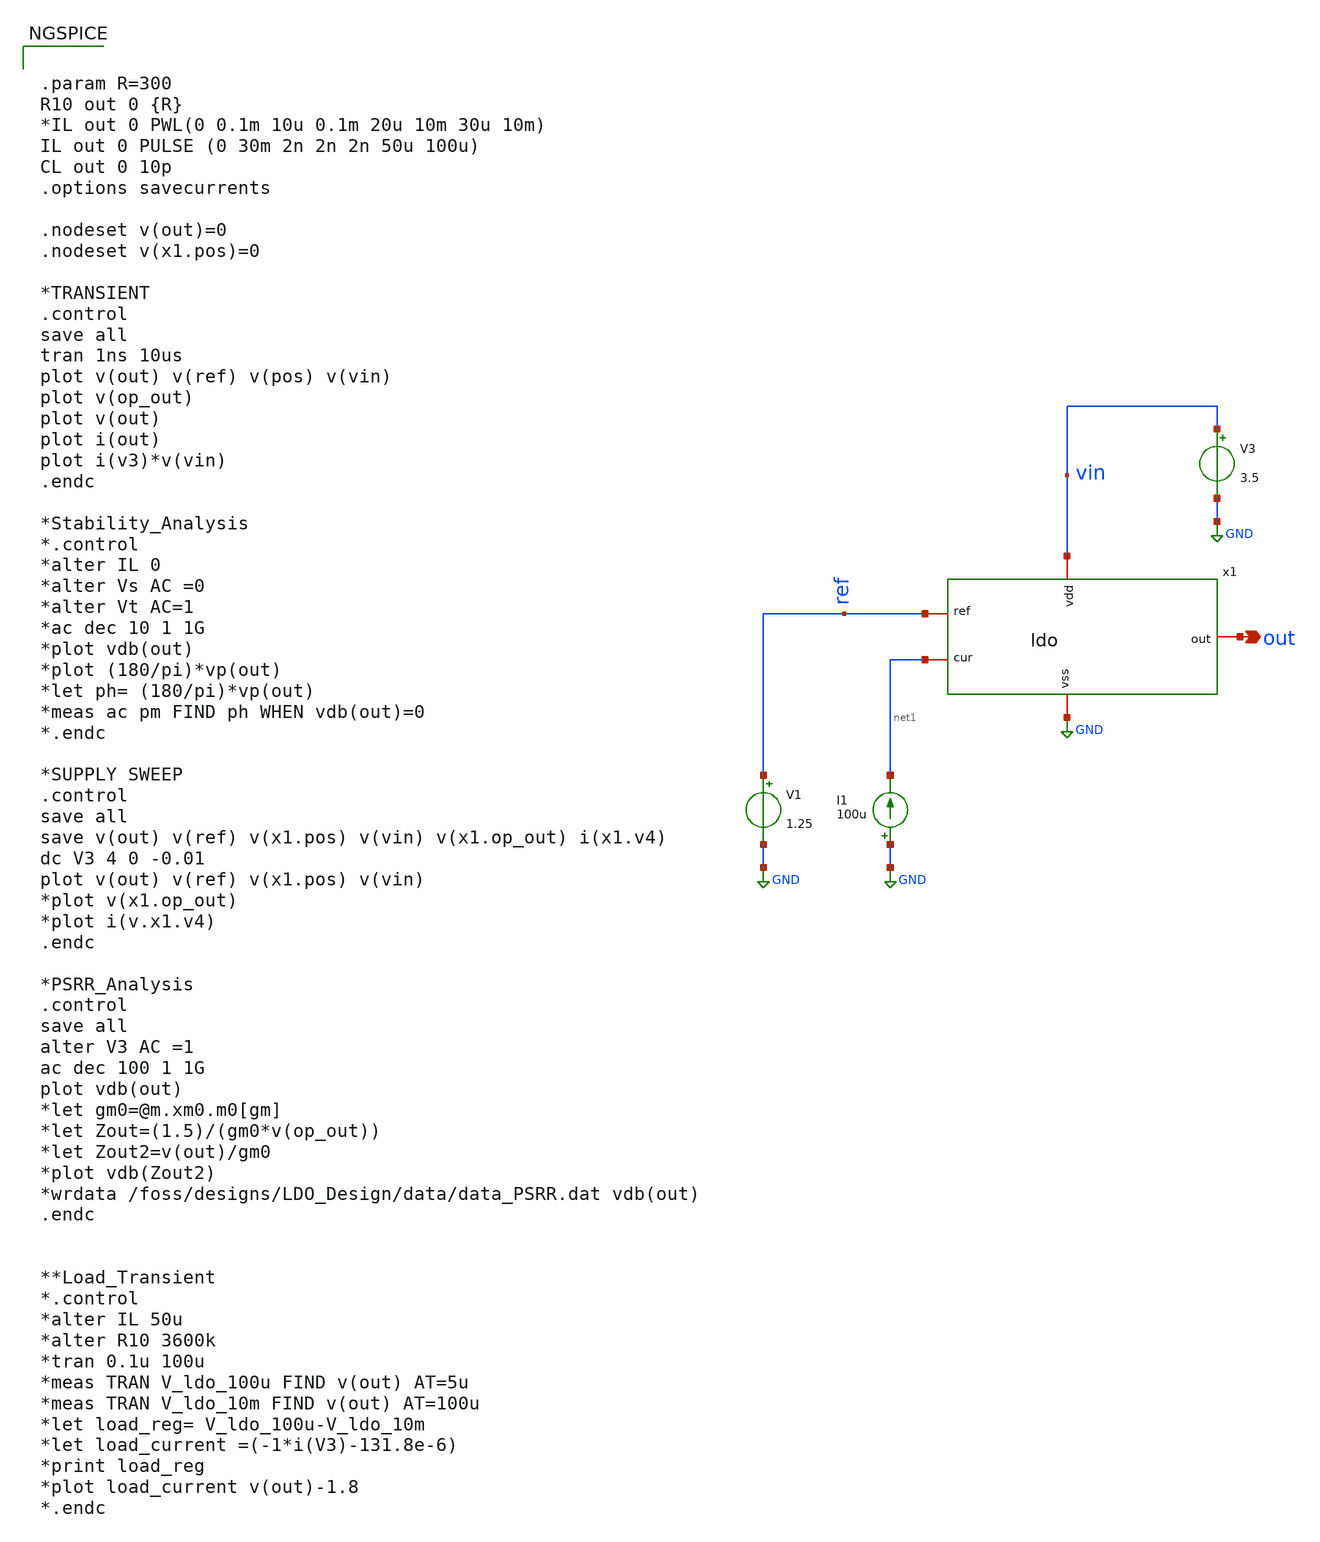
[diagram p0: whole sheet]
** sch_path: LDO/xschem/ldo/ldo-test.sch

.include $env(PDK_ROOT)/$env(PDK)/libs.tech/ngspice/design.ngspice
.lib $env(PDK_ROOT)/$env(PDK)/libs.tech/ngspice/sm141064.ngspice typical
.lib $env(PDK_ROOT)/$env(PDK)/libs.tech/ngspice/sm141064.ngspice mimcap_statistical
.lib $env(PDK_ROOT)/$env(PDK)/libs.tech/ngspice/sm141064.ngspice cap_mim
.lib $env(PDK_ROOT)/$env(PDK)/libs.tech/ngspice/sm141064.ngspice res_typical

**.subckt ldo-test out
*.opin out
I1 GND net1 100u
V1 ref GND 1.25
V3 vin GND 3.5
x1 vin ref net1 out GND ldo
**** begin user architecture code

.param R=300
R10 out 0 {R}
*IL out 0 PWL(0 0.1m 10u 0.1m 20u 10m 30u 10m)
IL out 0 PULSE (0 30m 2n 2n 2n 50u 100u)
CL out 0 10p
.options savecurrents

.nodeset v(out)=0
.nodeset v(x1.pos)=0

*TRANSIENT
.control
save all
tran 1ns 10us
plot v(out) v(ref) v(pos) v(vin)
plot v(op_out)
plot v(out)
plot i(out)
plot i(v3)*v(vin)
.endc

*Stability_Analysis
*.control
*alter IL 0
*alter Vs AC =0
*alter Vt AC=1
*ac dec 10 1 1G
*plot vdb(out)
*plot (180/pi)*vp(out)
*let ph= (180/pi)*vp(out)
*meas ac pm FIND ph WHEN vdb(out)=0
*.endc

*SUPPLY SWEEP
.control
save all
save v(out) v(ref) v(x1.pos) v(vin) v(x1.op_out) i(x1.v4)
dc V3 4 0 -0.01
plot v(out) v(ref) v(x1.pos) v(vin)
*plot v(x1.op_out)
*plot i(v.x1.v4)
.endc

*PSRR_Analysis
.control
save all
alter V3 AC =1
ac dec 100 1 1G
plot vdb(out)
*let gm0=@m.xm0.m0[gm]
*let Zout=(1.5)/(gm0*v(op_out))
*let Zout2=v(out)/gm0
*plot vdb(Zout2)
*wrdata /foss/designs/LDO_Design/data/data_PSRR.dat vdb(out)
.endc


**Load_Transient
*.control
*alter IL 50u
*alter R10 3600k
*tran 0.1u 100u
*meas TRAN V_ldo_100u FIND v(out) AT=5u
*meas TRAN V_ldo_10m FIND v(out) AT=100u
*let load_reg= V_ldo_100u-V_ldo_10m
*let load_current =(-1*i(V3)-131.8e-6)
*print load_reg
*plot load_current v(out)-1.8
*.endc

**** end user architecture code
**.ends

* expanding   symbol:  ldo.sym # of pins=5
** sym_path: LDO/xschem/ldo/ldo.sym
** sch_path: LDO/xschem/ldo/ldo.sch
.subckt ldo vdd ref cur out vss
*.iopin ref
*.iopin out
*.iopin cur
*.iopin vss
*.iopin vdd
X1 vdd op_out ref pos cur vss ota-ldo
XM1 out op_out vdd vdd pfet_03v3 L=1u W=100u nf=1 ad='int((nf+1)/2) * W/nf * 0.18u' as='int((nf+2)/2) * W/nf * 0.18u'
+ pd='2*int((nf+1)/2) * (W/nf + 0.18u)' ps='2*int((nf+2)/2) * (W/nf + 0.18u)' nrd='0.18u / W' nrs='0.18u / W'
+ sa=0 sb=0 sd=0 m=30
XR1 net1 out vss ppolyf_u_1k r_width=1e-6 r_length=164e-6 m=1
XR2 vss pos vss ppolyf_u_1k r_width=1e-6 r_length=120e-6 m=1
v4 net1 pos 0
.ends


* expanding   symbol:  ../ota-ldo/ota-ldo.sym # of pins=6
** sym_path: LDO/xschem/ota-ldo/ota-ldo.sym
** sch_path: LDO/xschem/ota-ldo/ota-ldo.sch
.subckt ota-ldo avdd out neg pos vb agnd
*.iopin vb
*.iopin avdd
*.iopin agnd
*.ipin neg
*.ipin pos
*.opin out
XC2 net2 out cap_mim_1f5fF c_width=50e-6 c_length=20e-6 m=1
XM1 net1 neg net3 agnd nfet_03v3 L=0.3u W=10u nf=1 ad='int((nf+1)/2) * W/nf * 0.18u' as='int((nf+2)/2) * W/nf * 0.18u'
+ pd='2*int((nf+1)/2) * (W/nf + 0.18u)' ps='2*int((nf+2)/2) * (W/nf + 0.18u)' nrd='0.18u / W' nrs='0.18u / W'
+ sa=0 sb=0 sd=0 m=1
XM3 net1 net1 avdd avdd pfet_03v3 L=0.8u W=9u nf=1 ad='int((nf+1)/2) * W/nf * 0.18u' as='int((nf+2)/2) * W/nf * 0.18u'
+ pd='2*int((nf+1)/2) * (W/nf + 0.18u)' ps='2*int((nf+2)/2) * (W/nf + 0.18u)' nrd='0.18u / W' nrs='0.18u / W'
+ sa=0 sb=0 sd=0 m=1
XM2 net2 pos net3 agnd nfet_03v3 L=0.3u W=10u nf=1 ad='int((nf+1)/2) * W/nf * 0.18u' as='int((nf+2)/2) * W/nf * 0.18u'
+ pd='2*int((nf+1)/2) * (W/nf + 0.18u)' ps='2*int((nf+2)/2) * (W/nf + 0.18u)' nrd='0.18u / W' nrs='0.18u / W'
+ sa=0 sb=0 sd=0 m=1
XM4 net2 net1 avdd avdd pfet_03v3 L=0.8u W=9u nf=1 ad='int((nf+1)/2) * W/nf * 0.18u' as='int((nf+2)/2) * W/nf * 0.18u'
+ pd='2*int((nf+1)/2) * (W/nf + 0.18u)' ps='2*int((nf+2)/2) * (W/nf + 0.18u)' nrd='0.18u / W' nrs='0.18u / W'
+ sa=0 sb=0 sd=0 m=1
XM7 net3 vb agnd agnd nfet_03v3 L=0.8u W=16u nf=1 ad='int((nf+1)/2) * W/nf * 0.18u' as='int((nf+2)/2) * W/nf * 0.18u'
+ pd='2*int((nf+1)/2) * (W/nf + 0.18u)' ps='2*int((nf+2)/2) * (W/nf + 0.18u)' nrd='0.18u / W' nrs='0.18u / W'
+ sa=0 sb=0 sd=0 m=1
XM8 vb vb agnd agnd nfet_03v3 L=0.8u W=1.66u nf=1 ad='int((nf+1)/2) * W/nf * 0.18u' as='int((nf+2)/2) * W/nf * 0.18u'
+ pd='2*int((nf+1)/2) * (W/nf + 0.18u)' ps='2*int((nf+2)/2) * (W/nf + 0.18u)' nrd='0.18u / W' nrs='0.18u / W'
+ sa=0 sb=0 sd=0 m=1
XM5 out net2 avdd avdd pfet_03v3 L=0.4u W=60u nf=1 ad='int((nf+1)/2) * W/nf * 0.18u' as='int((nf+2)/2) * W/nf * 0.18u'
+ pd='2*int((nf+1)/2) * (W/nf + 0.18u)' ps='2*int((nf+2)/2) * (W/nf + 0.18u)' nrd='0.18u / W' nrs='0.18u / W'
+ sa=0 sb=0 sd=0 m=1
XM6 out vb agnd agnd nfet_03v3 L=0.8u W=60u nf=1 ad='int((nf+1)/2) * W/nf * 0.18u' as='int((nf+2)/2) * W/nf * 0.18u'
+ pd='2*int((nf+1)/2) * (W/nf + 0.18u)' ps='2*int((nf+2)/2) * (W/nf + 0.18u)' nrd='0.18u / W' nrs='0.18u / W'
+ sa=0 sb=0 sd=0 m=1
.ends

.GLOBAL GND
.end
